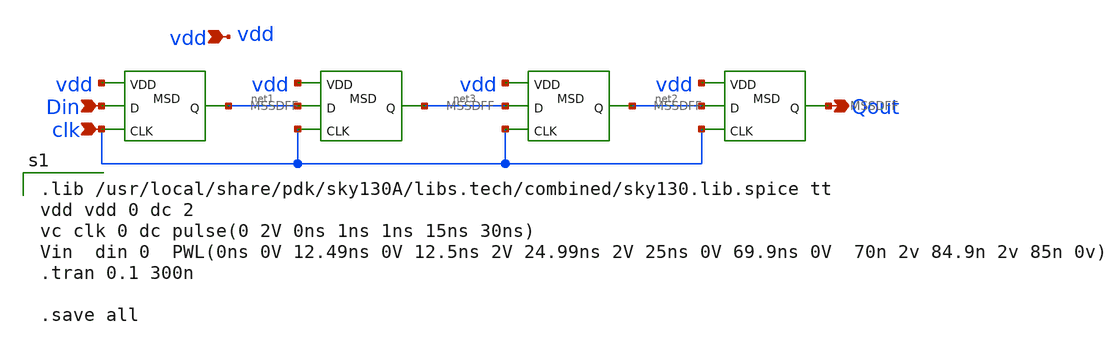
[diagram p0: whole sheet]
** sch_path: Circuit Files/circuits/circuits/SISO.sch
**.subckt SISO Qout Din vdd clk
*.opin Qout
*.ipin Din
*.ipin vdd
*.ipin clk
x1 net1 vdd Din clk MSSDFF
x2 net3 vdd net1 clk MSSDFF
x3 net2 vdd net3 clk MSSDFF
x4 Qout vdd net2 clk MSSDFF
**** begin user architecture code

.lib /usr/local/share/pdk/sky130A/libs.tech/combined/sky130.lib.spice tt
vdd vdd 0 dc 2
vc clk 0 dc pulse(0 2V 0ns 1ns 1ns 15ns 30ns)
Vin  din 0  PWL(0ns 0V 12.49ns 0V 12.5ns 2V 24.99ns 2V 25ns 0V 69.9ns 0V  70n 2v 84.9n 2v 85n 0v)
.tran 0.1 300n

.save all


**** end user architecture code
**.ends

* expanding   symbol:  daVLSI_World/circuits/MSSDFF.sym # of pins=4
** sym_path: Circuit Files/circuits/circuits/MSSDFF.sym
** sch_path: Circuit Files/circuits/circuits/MSSDFF.sch
.subckt MSSDFF Q VDD D CLK
*.ipin D
*.opin Q
*.ipin CLK
*.ipin VDD
x2 VDD D net2 CLK DFF1
x1 VDD net2 Q net1 DFF1
x3 net3 net4 net5 inverter_vtc
.ends


* expanding   symbol:  daVLSI_World/circuits/DFF1.sym # of pins=4
** sym_path: Circuit Files/circuits/circuits/DFF1.sym
** sch_path: Circuit Files/circuits/circuits/DFF1.sch
.subckt DFF1 vdd D Q clk
*.ipin clk
*.ipin D
*.ipin vdd
*.opin Q
x1 vdd net3 D clk GND NAND_gate
x3 vdd Q net3 net1 GND NAND_gate
x4 vdd net4 clk net2 GND NAND_gate
x5 vdd net1 Q net4 GND NAND_gate
x9 net5 net6 net7 inverter_vtc
**** begin user architecture code


.IC V(Q)=0


**** end user architecture code
.ends


* expanding   symbol:  daVLSI_World/gates/inverter_vtc.sym # of pins=3
** sym_path: Circuit Files/Logic gate design using MOSFETS/gates/inverter_vtc.sym
** sch_path: Circuit Files/Logic gate design using MOSFETS/gates/inverter_vtc.sch
.subckt inverter_vtc vdd vin vout
*.ipin vin
*.opin vout
*.ipin vdd
XM1 vout vin GND GND sky130_fd_pr__nfet_01v8 L=0.15 W=1 nf=1 ad='int((nf+1)/2) * W/nf * 0.29' as='int((nf+2)/2) * W/nf * 0.29'
+ pd='2*int((nf+1)/2) * (W/nf + 0.29)' ps='2*int((nf+2)/2) * (W/nf + 0.29)' nrd='0.29 / W' nrs='0.29 / W'
+ sa=0 sb=0 sd=0 mult=1 m=1
XM2 vout vin vdd vdd sky130_fd_pr__pfet_01v8 L=0.15 W=2 nf=1 ad='int((nf+1)/2) * W/nf * 0.29' as='int((nf+2)/2) * W/nf * 0.29'
+ pd='2*int((nf+1)/2) * (W/nf + 0.29)' ps='2*int((nf+2)/2) * (W/nf + 0.29)' nrd='0.29 / W' nrs='0.29 / W'
+ sa=0 sb=0 sd=0 mult=1 m=1
.ends


* expanding   symbol:  daVLSI_World/gates/NAND_gate.sym # of pins=5
** sym_path: Circuit Files/Logic gate design using MOSFETS/gates/NAND_gate.sym
** sch_path: Circuit Files/Logic gate design using MOSFETS/gates/NAND_gate.sch
.subckt NAND_gate vdd Y A B gnd
*.ipin A
*.ipin B
*.opin Y
*.ipin vdd
*.ipin gnd
XM1 Y A net1 gnd sky130_fd_pr__nfet_01v8 L=0.15 W=1 nf=1 ad='int((nf+1)/2) * W/nf * 0.29' as='int((nf+2)/2) * W/nf * 0.29'
+ pd='2*int((nf+1)/2) * (W/nf + 0.29)' ps='2*int((nf+2)/2) * (W/nf + 0.29)' nrd='0.29 / W' nrs='0.29 / W'
+ sa=0 sb=0 sd=0 mult=1 m=1
XM2 net1 B gnd gnd sky130_fd_pr__nfet_01v8 L=0.15 W=1 nf=1 ad='int((nf+1)/2) * W/nf * 0.29' as='int((nf+2)/2) * W/nf * 0.29'
+ pd='2*int((nf+1)/2) * (W/nf + 0.29)' ps='2*int((nf+2)/2) * (W/nf + 0.29)' nrd='0.29 / W' nrs='0.29 / W'
+ sa=0 sb=0 sd=0 mult=1 m=1
XM3 Y A vdd vdd sky130_fd_pr__pfet_01v8 L=0.15 W=2 nf=1 ad='int((nf+1)/2) * W/nf * 0.29' as='int((nf+2)/2) * W/nf * 0.29'
+ pd='2*int((nf+1)/2) * (W/nf + 0.29)' ps='2*int((nf+2)/2) * (W/nf + 0.29)' nrd='0.29 / W' nrs='0.29 / W'
+ sa=0 sb=0 sd=0 mult=1 m=1
XM4 Y B vdd vdd sky130_fd_pr__pfet_01v8 L=0.15 W=2 nf=1 ad='int((nf+1)/2) * W/nf * 0.29' as='int((nf+2)/2) * W/nf * 0.29'
+ pd='2*int((nf+1)/2) * (W/nf + 0.29)' ps='2*int((nf+2)/2) * (W/nf + 0.29)' nrd='0.29 / W' nrs='0.29 / W'
+ sa=0 sb=0 sd=0 mult=1 m=1
.ends

.GLOBAL GND
.end
